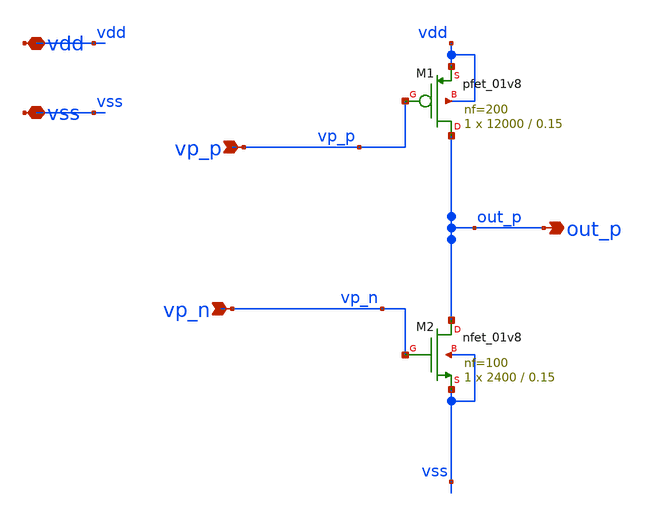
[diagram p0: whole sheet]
** sch_path: xschem/src/output_driver/half_driver.sch
**.subckt half_driver vp_p vp_n out_p vdd vss
*.ipin vp_p
*.ipin vp_n
*.opin out_p
*.iopin vdd
*.iopin vss
XM1 out_p vp_p vdd vdd sky130_fd_pr__pfet_01v8 L=0.15 W=12000 nf=200 ad='int((nf+1)/2) * W/nf * 0.29'
+ as='int((nf+2)/2) * W/nf * 0.29' pd='2*int((nf+1)/2) * (W/nf + 0.29)' ps='2*int((nf+2)/2) * (W/nf + 0.29)'
+ nrd='0.29 / W' nrs='0.29 / W' sa=0 sb=0 sd=0 mult=1 m=1
XM2 out_p vp_n vss vss sky130_fd_pr__nfet_01v8 L=0.15 W=2400 nf=100 ad='int((nf+1)/2) * W/nf * 0.29'
+ as='int((nf+2)/2) * W/nf * 0.29' pd='2*int((nf+1)/2) * (W/nf + 0.29)' ps='2*int((nf+2)/2) * (W/nf + 0.29)'
+ nrd='0.29 / W' nrs='0.29 / W' sa=0 sb=0 sd=0 mult=1 m=1
**.ends
.end
